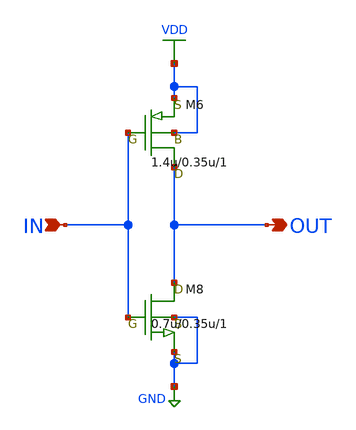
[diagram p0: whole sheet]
** sch_path: LR_hasegawa/LR_Work2/symbol/INVERTER_MIN.sch
**.subckt INVERTER_MIN OUT IN
*.opin OUT
*.ipin IN
M6 OUT IN VDD VDD pch w=1.4u l=0.35u as=1.2p ps=4.6u ad=1.2p pd=4.6u m=1
M8 OUT IN GND GND nch w=0.7u l=0.35u as=0.56p ps=3u ad=0.56p pd=3u m=1
**.ends
.GLOBAL VDD
.GLOBAL GND
.end
